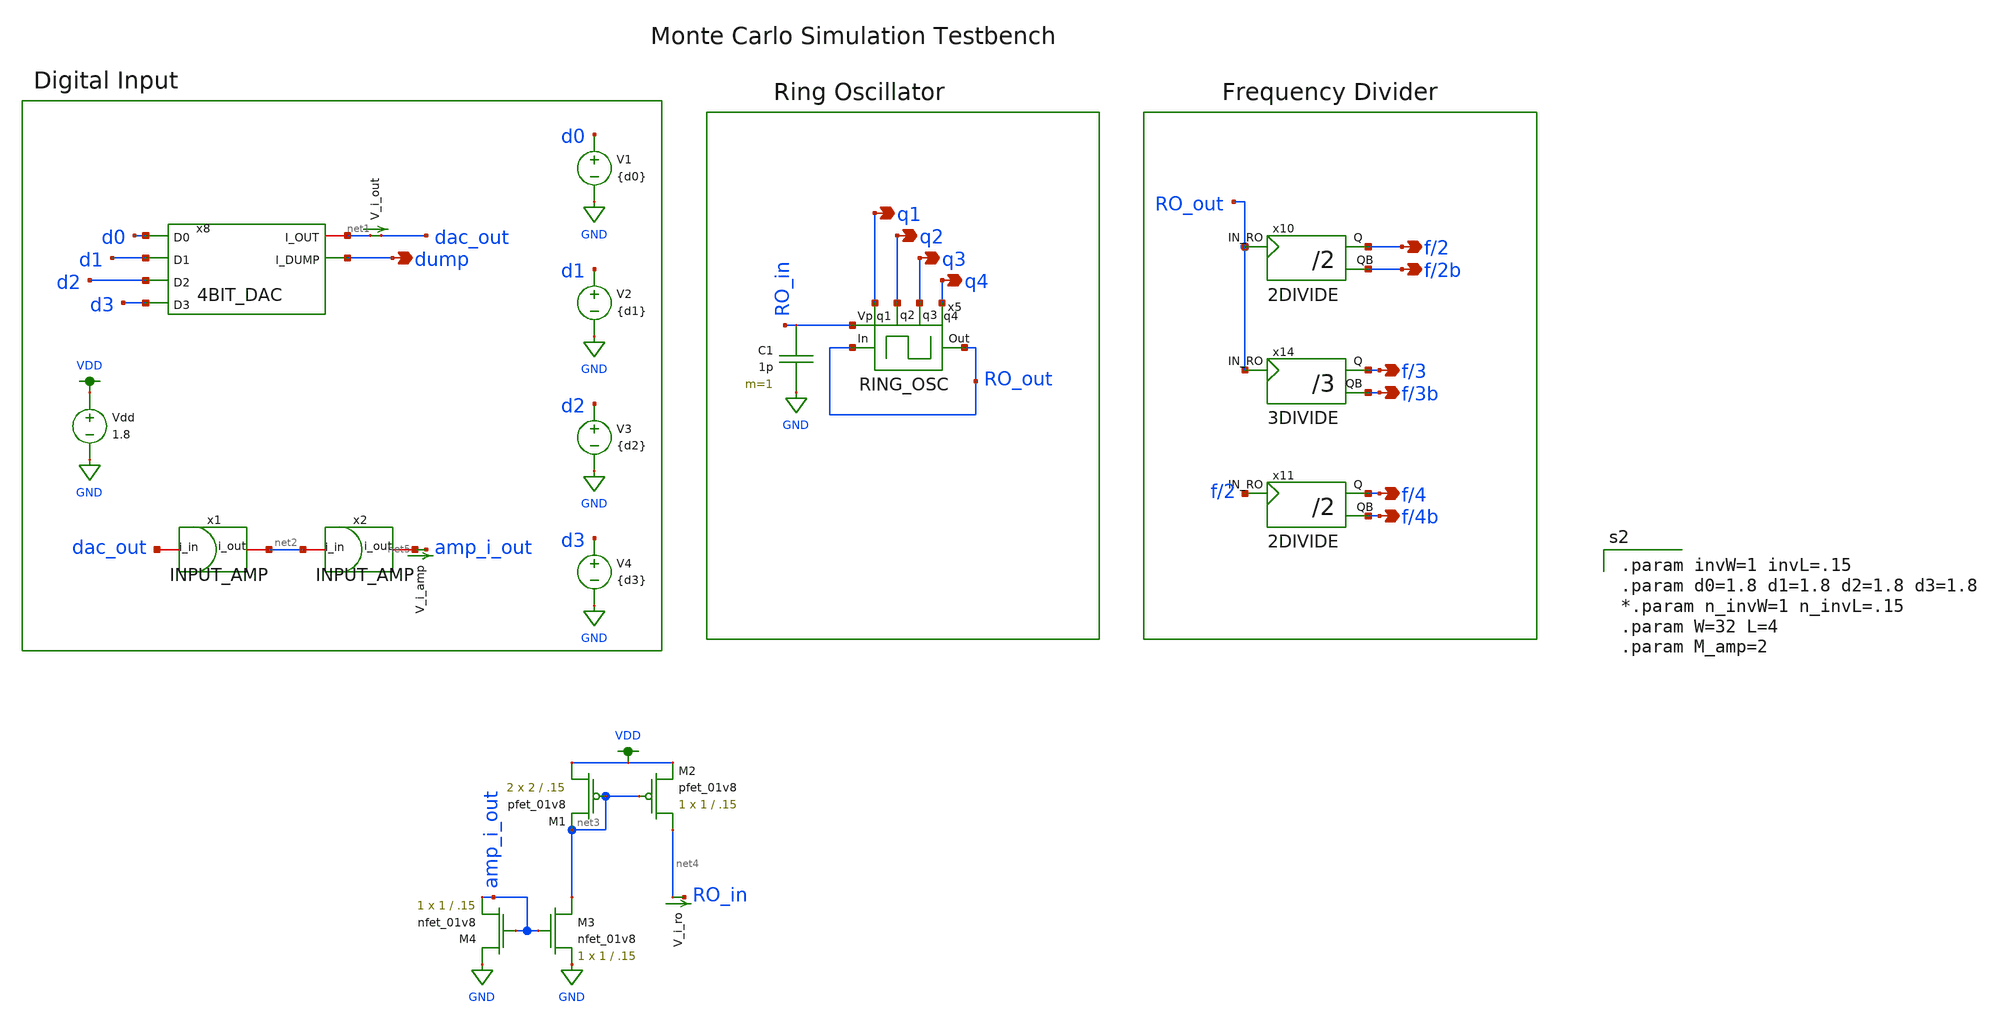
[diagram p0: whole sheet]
** sch_path: schemas/mc_testbench.sch
**.subckt mc_testbench dump f/2 f/4 f/3 f/3b f/4b f/2b q1 q2 q3 q4
*.opin dump
*.opin f/2
*.opin f/4
*.opin f/3
*.opin f/3b
*.opin f/4b
*.opin f/2b
*.opin q1
*.opin q2
*.opin q3
*.opin q4
x8 net1 dump d1 d0 d2 d3 4BIT_DAC
x10 f/2 f/2b RO_out 2DIVIDE
x11 f/4 f/4b f/2 2DIVIDE
V_i_out net1 dac_out 0
.save i(v_i_out)
x14 f/3 f/3b RO_out 3DIVIDE
V2 d1 GND {d1}
V1 d0 GND {d0}
V3 d2 GND {d2}
V4 d3 GND {d3}
x1 dac_out net2 INPUT_AMP
x2 net2 net5 INPUT_AMP
x5 q4 q1 q2 q3 RO_out RO_out RO_in RING_OSC
V_i_ro net4 RO_in 0
.save i(v_i_ro)
Vdd VDD GND 1.8
XM1 VDD net3 net3 VDD sky130_fd_pr__pfet_01v8 L=.15 W=2 nf=1 ad='int((nf+1)/2) * W/nf * 0.29' as='int((nf+2)/2) * W/nf * 0.29'
+ pd='2*int((nf+1)/2) * (W/nf + 0.29)' ps='2*int((nf+2)/2) * (W/nf + 0.29)' nrd='0.29 / W' nrs='0.29 / W'
+ sa=0 sb=0 sd=0 mult=2 m=2
XM2 net4 net3 VDD VDD sky130_fd_pr__pfet_01v8 L=.15 W=1 nf=1 ad='int((nf+1)/2) * W/nf * 0.29' as='int((nf+2)/2) * W/nf * 0.29'
+ pd='2*int((nf+1)/2) * (W/nf + 0.29)' ps='2*int((nf+2)/2) * (W/nf + 0.29)' nrd='0.29 / W' nrs='0.29 / W'
+ sa=0 sb=0 sd=0 mult=1 m=1
XM3 net3 amp_i_out GND GND sky130_fd_pr__nfet_01v8 L=.15 W=1 nf=1 ad='int((nf+1)/2) * W/nf * 0.29' as='int((nf+2)/2) * W/nf * 0.29'
+ pd='2*int((nf+1)/2) * (W/nf + 0.29)' ps='2*int((nf+2)/2) * (W/nf + 0.29)' nrd='0.29 / W' nrs='0.29 / W'
+ sa=0 sb=0 sd=0 mult=1 m=1
XM4 GND amp_i_out amp_i_out GND sky130_fd_pr__nfet_01v8 L=.15 W=1 nf=1 ad='int((nf+1)/2) * W/nf * 0.29'
+ as='int((nf+2)/2) * W/nf * 0.29' pd='2*int((nf+1)/2) * (W/nf + 0.29)' ps='2*int((nf+2)/2) * (W/nf + 0.29)'
+ nrd='0.29 / W' nrs='0.29 / W' sa=0 sb=0 sd=0 mult=1 m=1
C1 RO_in GND 1p m=1
V_i_amp net5 amp_i_out 0
.save i(v_i_amp)
**** begin user architecture code

.option wnflag=1
.lib ~/skywater/skywater-pdk/libraries/sky130_fd_pr_ngspice/latest/models/sky130.lib.spice tt





.control
    set wr_singlescale
    let runs = 10
    let run = 1
    while run <= runs
        set appendwrite = FALSE
        set wr_vecnames
        let code = 0
        while code < 32
            if code eq 0
                let D0 = 0
            else
                let D0 = code % 2
            end
            if floor(code / 2 ) eq 0
                let D1 = 0
            else
                let D1 = floor(code / 2 ) % 2
            end
            if floor(code / 4 ) eq 0
                let D2 = 0
            else
                let D2 = floor(code / 4 ) % 2
            end
            if floor(code / 8 ) eq 0
                let D3 = 0
            else
                let D3 = floor(code / 8 ) % 2
            end

            alter V1 $&D0
            alter V2 $&D1
            alter V3 $&D2
            alter V4 $&D3

            save all
            op
            write ./schemas/simulation/MCDACDATA{$&run}.csv v(D0) v(D1) v(D2) v(D3) i(v_i_out) v(dac_out)
            if code eq 0
                set appendwrite
                set wr_vecnames = FALSE
            end
            let code = code + 1
        end
        reset
        let run = run + 1
    end
    quit
.endc


.param invW=1 invL=.15
.param d0=1.8 d1=1.8 d2=1.8 d3=1.8
*.param n_invW=1 n_invL=.15
.param W=32 L=4
.param M_amp=2


**** end user architecture code
**.ends
.GLOBAL GND
.GLOBAL VDD
.end
